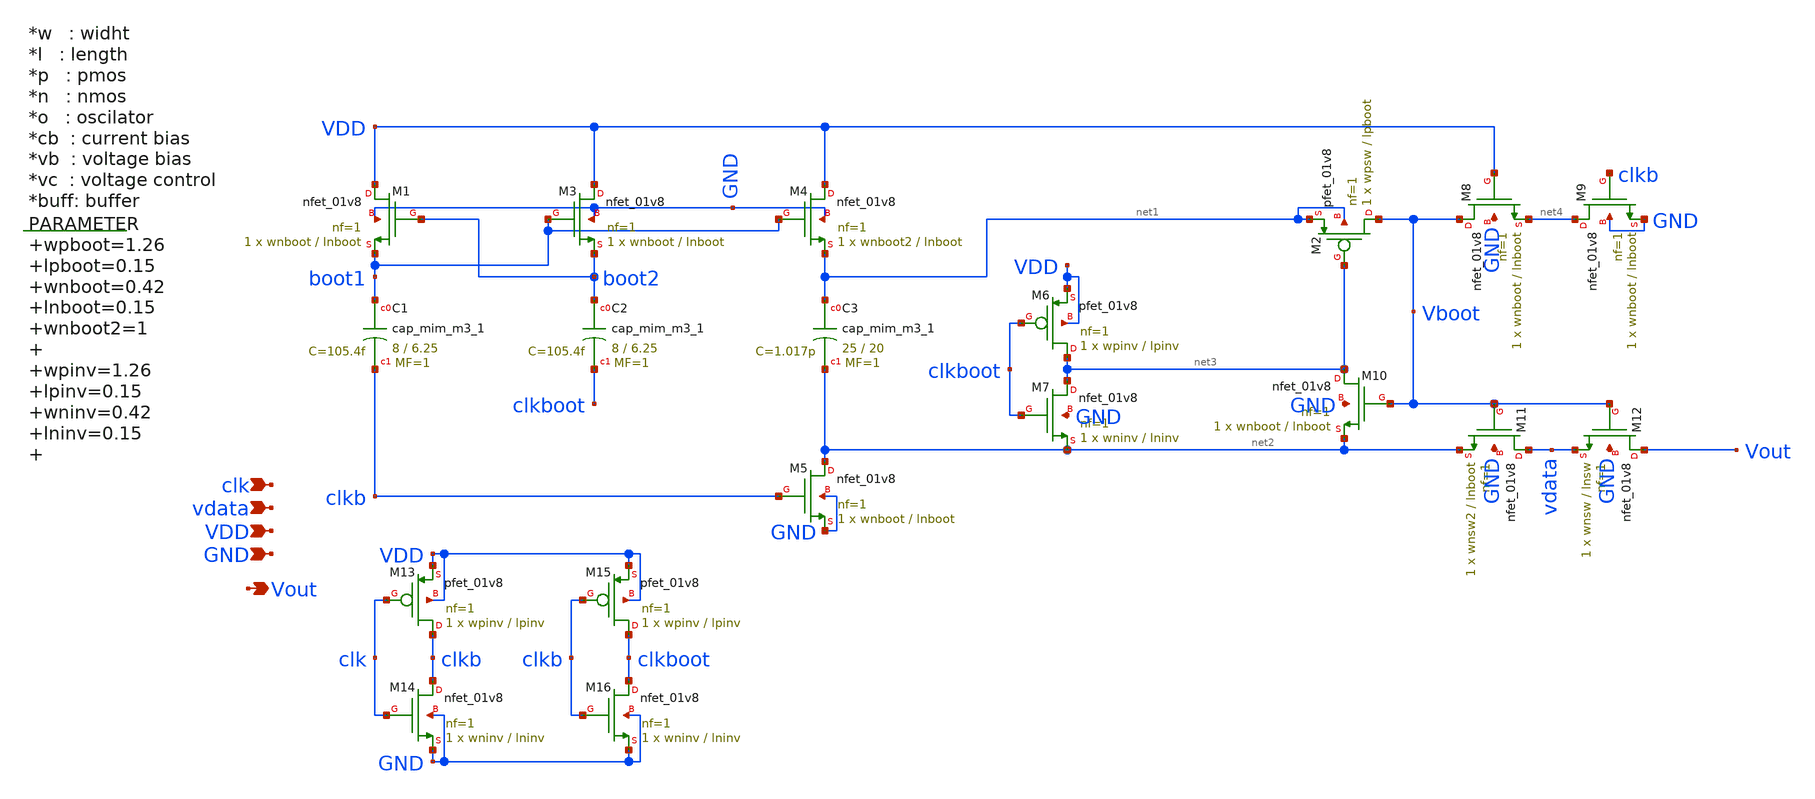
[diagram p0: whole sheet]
** sch_path: xschem/t_h_bootstrap_switch.sch
**.subckt t_h_bootstrap_switch clk Vout vdata VDD GND
*.ipin clk
*.opin Vout
*.ipin vdata
*.ipin VDD
*.ipin GND
.param wpboot=1.26 lpboot=0.15 wnboot=0.42 lnboot=0.15 wnboot2=1 wpinv=1.26 lpinv=0.15 wninv=0.42
+ lninv=0.15 wcboot=8 lcboot=6.25 wnsw=5 lnsw=0.3 wnsw2=1 wpsw=2


XM1 VDD boot2 boot1 GND sky130_fd_pr__nfet_01v8 L=lnboot W=wnboot nf=1 ad='int((nf+1)/2) * W/nf * 0.29'
+ as='int((nf+2)/2) * W/nf * 0.29' pd='2*int((nf+1)/2) * (W/nf + 0.29)' ps='2*int((nf+2)/2) * (W/nf + 0.29)'
+ nrd='0.29 / W' nrs='0.29 / W' sa=0 sb=0 sd=0 mult=1 m=1
XM2 Vboot net3 net1 net1 sky130_fd_pr__pfet_01v8 L=lpboot W=wpsw nf=1 ad='int((nf+1)/2) * W/nf * 0.29'
+ as='int((nf+2)/2) * W/nf * 0.29' pd='2*int((nf+1)/2) * (W/nf + 0.29)' ps='2*int((nf+2)/2) * (W/nf + 0.29)'
+ nrd='0.29 / W' nrs='0.29 / W' sa=0 sb=0 sd=0 mult=1 m=1
XC1 boot1 clkb sky130_fd_pr__cap_mim_m3_1 W=8 L=6.25 MF=1 m=1
XC2 boot2 clkboot sky130_fd_pr__cap_mim_m3_1 W=8 L=6.25 MF=1 m=1
XM4 VDD boot1 net1 GND sky130_fd_pr__nfet_01v8 L=lnboot W=wnboot2 nf=1 ad='int((nf+1)/2) * W/nf * 0.29'
+ as='int((nf+2)/2) * W/nf * 0.29' pd='2*int((nf+1)/2) * (W/nf + 0.29)' ps='2*int((nf+2)/2) * (W/nf + 0.29)'
+ nrd='0.29 / W' nrs='0.29 / W' sa=0 sb=0 sd=0 mult=1 m=1
XM5 net2 clkb GND GND sky130_fd_pr__nfet_01v8 L=lnboot W=wnboot nf=1 ad='int((nf+1)/2) * W/nf * 0.29'
+ as='int((nf+2)/2) * W/nf * 0.29' pd='2*int((nf+1)/2) * (W/nf + 0.29)' ps='2*int((nf+2)/2) * (W/nf + 0.29)'
+ nrd='0.29 / W' nrs='0.29 / W' sa=0 sb=0 sd=0 mult=1 m=1
XC3 net1 net2 sky130_fd_pr__cap_mim_m3_1 W=25 L=20 MF=1 m=1
XM6 net3 clkboot VDD VDD sky130_fd_pr__pfet_01v8 L=lpinv W=wpinv nf=1 ad='int((nf+1)/2) * W/nf * 0.29'
+ as='int((nf+2)/2) * W/nf * 0.29' pd='2*int((nf+1)/2) * (W/nf + 0.29)' ps='2*int((nf+2)/2) * (W/nf + 0.29)'
+ nrd='0.29 / W' nrs='0.29 / W' sa=0 sb=0 sd=0 mult=1 m=1
XM7 net3 clkboot net2 GND sky130_fd_pr__nfet_01v8 L=lninv W=wninv nf=1 ad='int((nf+1)/2) * W/nf * 0.29'
+ as='int((nf+2)/2) * W/nf * 0.29' pd='2*int((nf+1)/2) * (W/nf + 0.29)' ps='2*int((nf+2)/2) * (W/nf + 0.29)'
+ nrd='0.29 / W' nrs='0.29 / W' sa=0 sb=0 sd=0 mult=1 m=1
XM8 Vboot VDD net4 GND sky130_fd_pr__nfet_01v8 L=lnboot W=wnboot nf=1 ad='int((nf+1)/2) * W/nf * 0.29'
+ as='int((nf+2)/2) * W/nf * 0.29' pd='2*int((nf+1)/2) * (W/nf + 0.29)' ps='2*int((nf+2)/2) * (W/nf + 0.29)'
+ nrd='0.29 / W' nrs='0.29 / W' sa=0 sb=0 sd=0 mult=1 m=1
XM9 net4 clkb GND GND sky130_fd_pr__nfet_01v8 L=lnboot W=wnboot nf=1 ad='int((nf+1)/2) * W/nf * 0.29'
+ as='int((nf+2)/2) * W/nf * 0.29' pd='2*int((nf+1)/2) * (W/nf + 0.29)' ps='2*int((nf+2)/2) * (W/nf + 0.29)'
+ nrd='0.29 / W' nrs='0.29 / W' sa=0 sb=0 sd=0 mult=1 m=1
XM10 net3 Vboot net2 GND sky130_fd_pr__nfet_01v8 L=lnboot W=wnboot nf=1 ad='int((nf+1)/2) * W/nf * 0.29'
+ as='int((nf+2)/2) * W/nf * 0.29' pd='2*int((nf+1)/2) * (W/nf + 0.29)' ps='2*int((nf+2)/2) * (W/nf + 0.29)'
+ nrd='0.29 / W' nrs='0.29 / W' sa=0 sb=0 sd=0 mult=1 m=1
XM11 vdata Vboot net2 GND sky130_fd_pr__nfet_01v8 L=lnboot W=wnsw2 nf=1 ad='int((nf+1)/2) * W/nf * 0.29'
+ as='int((nf+2)/2) * W/nf * 0.29' pd='2*int((nf+1)/2) * (W/nf + 0.29)' ps='2*int((nf+2)/2) * (W/nf + 0.29)'
+ nrd='0.29 / W' nrs='0.29 / W' sa=0 sb=0 sd=0 mult=1 m=1
XM12 Vout Vboot vdata GND sky130_fd_pr__nfet_01v8 L=lnsw W=wnsw nf=1 ad='int((nf+1)/2) * W/nf * 0.29'
+ as='int((nf+2)/2) * W/nf * 0.29' pd='2*int((nf+1)/2) * (W/nf + 0.29)' ps='2*int((nf+2)/2) * (W/nf + 0.29)'
+ nrd='0.29 / W' nrs='0.29 / W' sa=0 sb=0 sd=0 mult=1 m=1
XM13 clkb clk VDD VDD sky130_fd_pr__pfet_01v8 L=lpinv W=wpinv nf=1 ad='int((nf+1)/2) * W/nf * 0.29' as='int((nf+2)/2) * W/nf * 0.29'
+ pd='2*int((nf+1)/2) * (W/nf + 0.29)' ps='2*int((nf+2)/2) * (W/nf + 0.29)' nrd='0.29 / W' nrs='0.29 / W'
+ sa=0 sb=0 sd=0 mult=1 m=1
XM14 clkb clk GND GND sky130_fd_pr__nfet_01v8 L=lninv W=wninv nf=1 ad='int((nf+1)/2) * W/nf * 0.29' as='int((nf+2)/2) * W/nf * 0.29'
+ pd='2*int((nf+1)/2) * (W/nf + 0.29)' ps='2*int((nf+2)/2) * (W/nf + 0.29)' nrd='0.29 / W' nrs='0.29 / W'
+ sa=0 sb=0 sd=0 mult=1 m=1
XM15 clkboot clkb VDD VDD sky130_fd_pr__pfet_01v8 L=lpinv W=wpinv nf=1 ad='int((nf+1)/2) * W/nf * 0.29'
+ as='int((nf+2)/2) * W/nf * 0.29' pd='2*int((nf+1)/2) * (W/nf + 0.29)' ps='2*int((nf+2)/2) * (W/nf + 0.29)'
+ nrd='0.29 / W' nrs='0.29 / W' sa=0 sb=0 sd=0 mult=1 m=1
XM16 clkboot clkb GND GND sky130_fd_pr__nfet_01v8 L=lninv W=wninv nf=1 ad='int((nf+1)/2) * W/nf * 0.29'
+ as='int((nf+2)/2) * W/nf * 0.29' pd='2*int((nf+1)/2) * (W/nf + 0.29)' ps='2*int((nf+2)/2) * (W/nf + 0.29)'
+ nrd='0.29 / W' nrs='0.29 / W' sa=0 sb=0 sd=0 mult=1 m=1
XM3 VDD boot1 boot2 GND sky130_fd_pr__nfet_01v8 L=lnboot W=wnboot nf=1 ad='int((nf+1)/2) * W/nf * 0.29'
+ as='int((nf+2)/2) * W/nf * 0.29' pd='2*int((nf+1)/2) * (W/nf + 0.29)' ps='2*int((nf+2)/2) * (W/nf + 0.29)'
+ nrd='0.29 / W' nrs='0.29 / W' sa=0 sb=0 sd=0 mult=1 m=1
**.ends
.end
